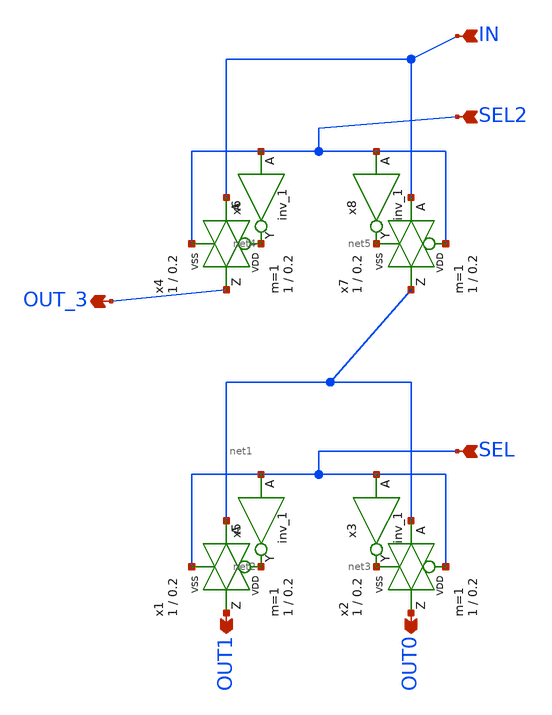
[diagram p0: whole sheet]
** sch_path: 1bit_adc/passgate_2_outputs.sch
**.subckt passgate_2_outputs OUT1 OUT0 SEL OUT_3 SEL2 IN
*.opin OUT1
*.opin OUT0
*.ipin SEL
*.opin OUT_3
*.ipin SEL2
*.ipin IN
x1 OUT1 net1 net2 SEL VDD VSS passgate W_N=1 L_N=0.2 W_P=1 L_P=0.2 m=1
x2 OUT0 net1 SEL net3 VDD VSS passgate W_N=1 L_N=0.2 W_P=1 L_P=0.2 m=1
x4 OUT_3 IN net4 SEL2 VDD VSS passgate W_N=1 L_N=0.2 W_P=1 L_P=0.2 m=1
x7 net1 IN SEL2 net5 VDD VSS passgate W_N=1 L_N=0.2 W_P=1 L_P=0.2 m=1
x5 SEL VGND VNB VPB VPWR net2 sky130_fd_sc_hd__inv_1
x3 SEL VGND VNB VPB VPWR net3 sky130_fd_sc_hd__inv_1
x8 SEL2 VGND VNB VPB VPWR net5 sky130_fd_sc_hd__inv_1
x6 SEL2 VGND VNB VPB VPWR net4 sky130_fd_sc_hd__inv_1
**** begin user architecture code

** opencircuitdesign pdks install
.lib $::SKYWATER_MODELS/sky130.lib.spice tt
.include $::SKYWATER_STDCELLS/sky130_fd_sc_hd.spice
.include /foss/pdks/sky130A/libs.tech/xschem/sky130_stdcells/

**** end user architecture code
**.ends

* expanding   symbol:  sky130_tests/passgate.sym # of pins=4
** sym_path: sky130_tests/passgate.sym
** sch_path: sky130_tests/passgate.sch
.subckt passgate Z A GP GN VCCBPIN VSSBPIN  W_N=1 L_N=0.2 W_P=1 L_P=0.2

*.iopin A
*.iopin Z
*.ipin GP
*.ipin GN
XM1 A GN Z VSS sky130_fd_pr__nfet_01v8 W=W_N L=L_N ad='W * 0.29' pd='W + 2 * 0.29' as='W * 0.29' ps='W + 2 * 0.29'
+ nrd=0 nrs=0 sa=0 sb=0 sd=0 nf=1 mult=1
XM2 A GP Z VCC sky130_fd_pr__pfet_01v8 W=W_P L=L_P ad='W * 0.29' pd='W + 2 * 0.29' as='W * 0.29' ps='W + 2 * 0.29'
+ nrd=0 nrs=0 sa=0 sb=0 sd=0 nf=1 mult=1
.ends

.end
